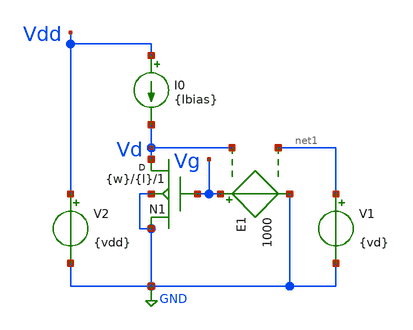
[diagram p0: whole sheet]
** sch_path: Parametros_Vaf/sigma_test.sch
**.subckt sigma_test
N1 Vd Vg GND GND NMOS_ACM w={w} l={l} m=1
E1 Vg GND Vd net1 1000
I0 Vdd Vd {Ibias}
V1 net1 GND {vd}
V2 Vdd GND {vdd}
**** begin user architecture code


* Circuit Parameters
.param vd = 3
.param vdd = 1.2
.param Ibias = 1m
.param step = 0.01
.param w = 5.0u
.param l = 0.18u
* Include Models
.model NMOS_ACM nmos_ACM
.model PMOS_ACM pmos_ACM
* OP Parameters & Singals to save
.save all
.save @n1[gm_op]
.save @n1[gmd_op]
*Simulations
.dc V1 0 {vd} {step}
.control
pre_osdi NMOS_ACM_2V0.osdi
pre_osdi PMOS_ACM_2V0.osdi
run
setplot dc1
plot @n1[gm_op] @n1[gmd_op]
let sigma = @n1[gmd_op]/@n1[gm_op]
set filetype = ascii
write dcsweep.raw
.endc
.end


**** end user architecture code
**.ends
.GLOBAL GND
.end
